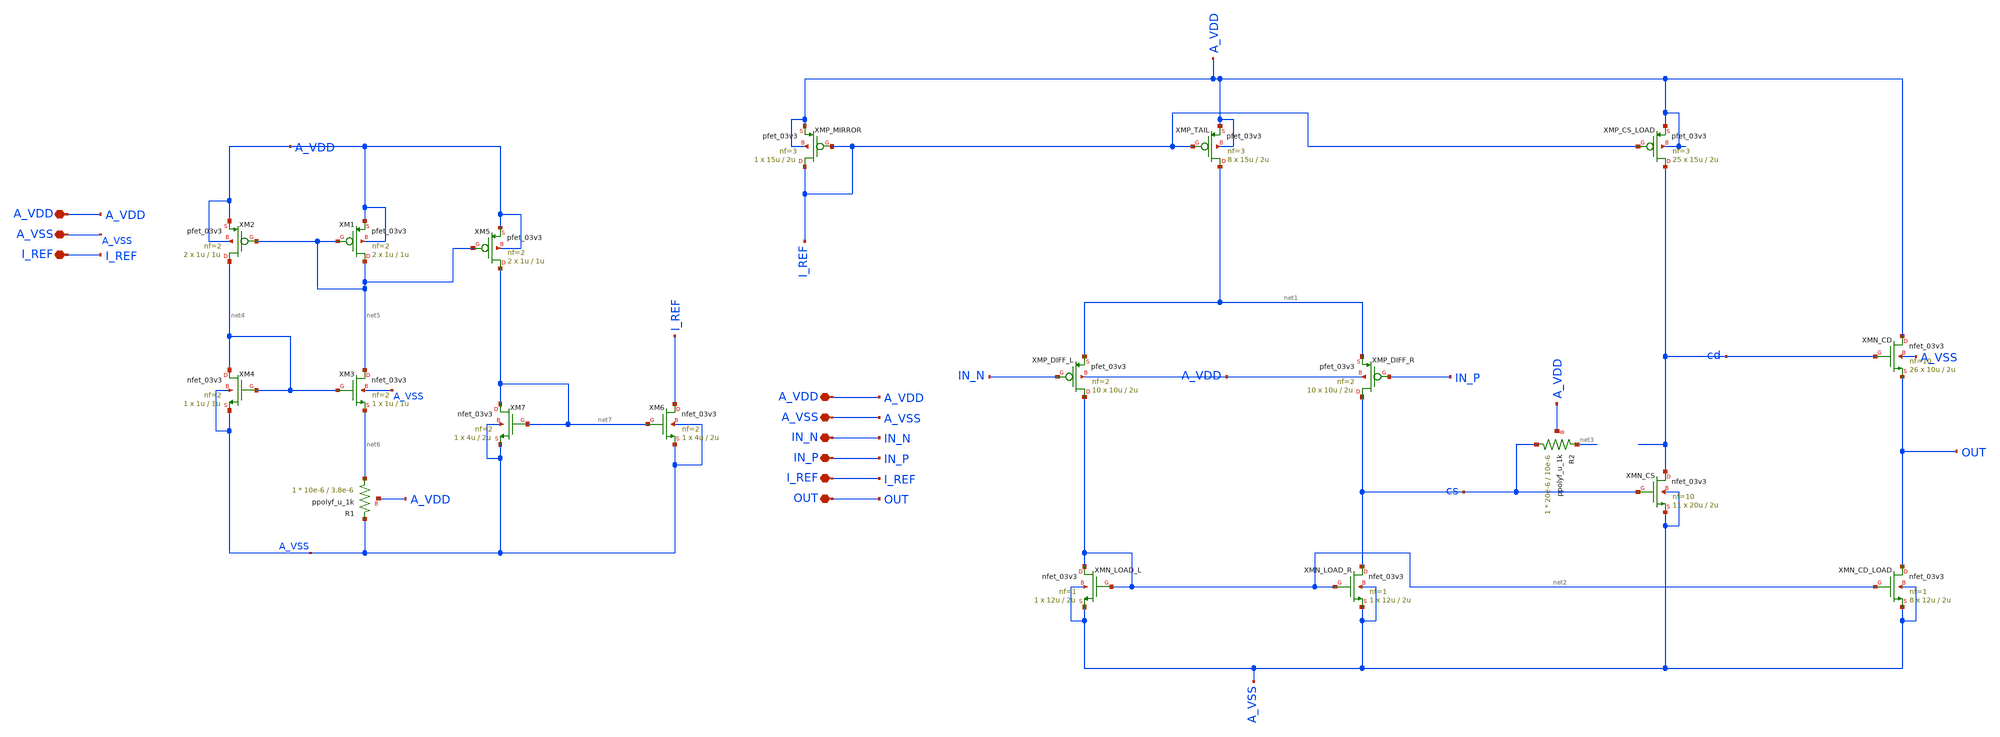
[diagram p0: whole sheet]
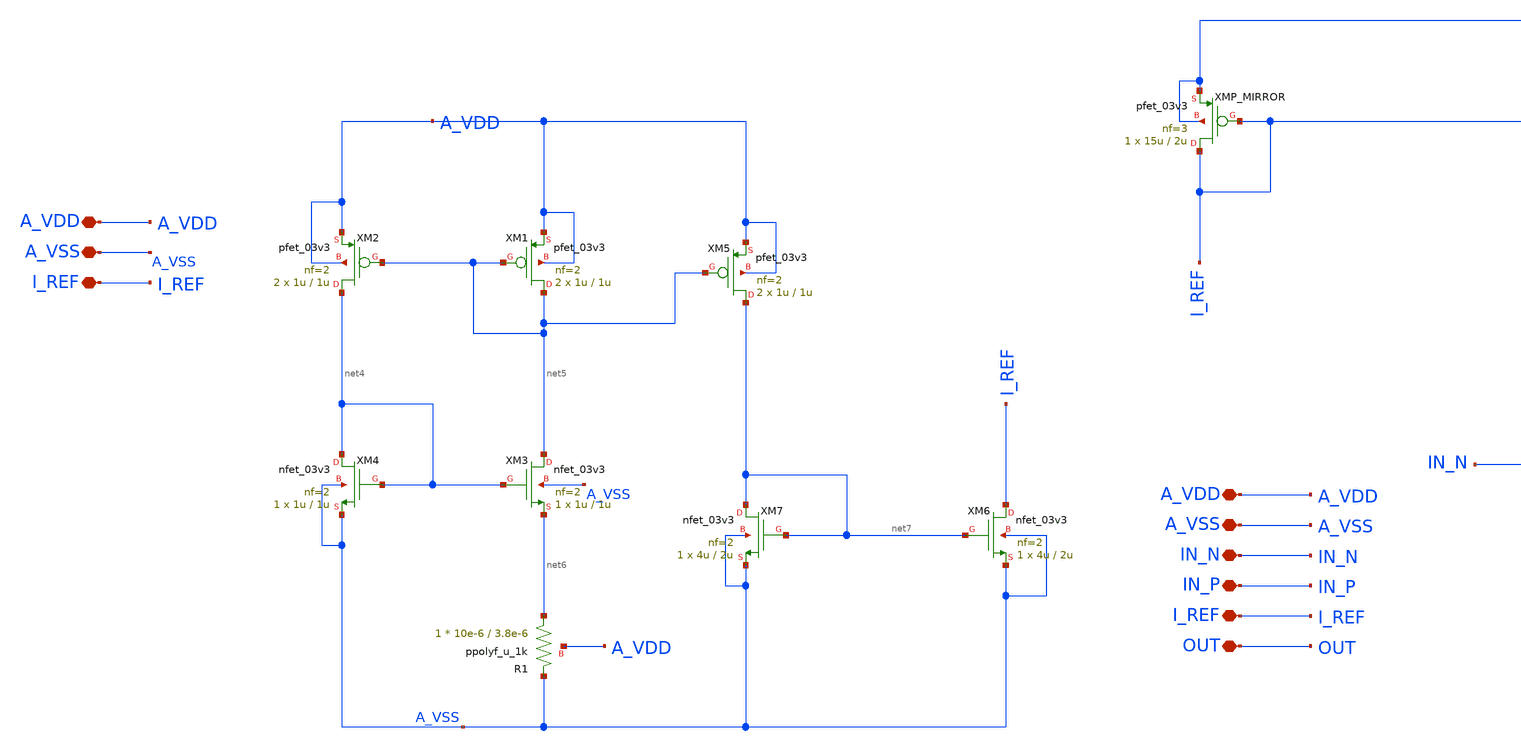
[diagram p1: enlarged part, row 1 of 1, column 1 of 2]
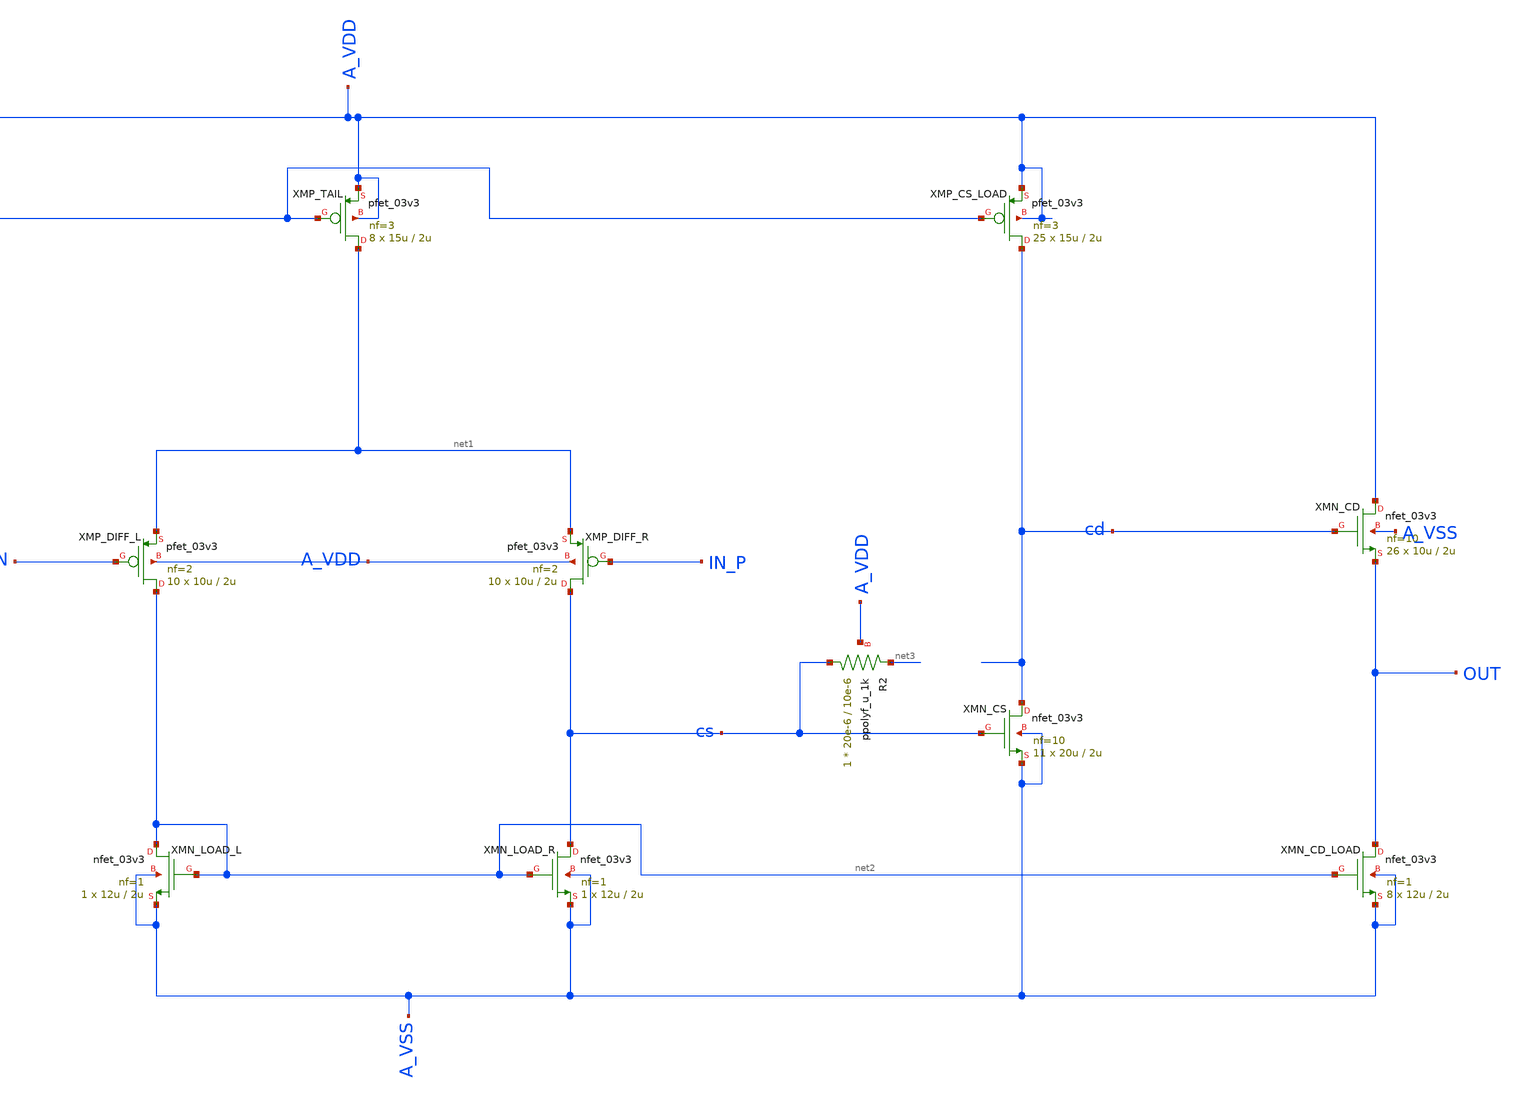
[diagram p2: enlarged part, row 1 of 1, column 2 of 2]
** sch_path: designs/libs/TIA/TIA_and_IREF.sch
**.subckt TIA_and_IREF A_VDD IN_N IN_P A_VSS I_REF OUT I_REF A_VSS A_VDD
*.iopin A_VDD
*.iopin IN_N
*.iopin IN_P
*.iopin A_VSS
*.iopin I_REF
*.iopin OUT
*.iopin I_REF
*.iopin A_VSS
*.iopin A_VDD
XMP_TAIL net1 I_REF A_VDD A_VDD pfet_03v3 L=2u W=15u nf=3 ad='int((nf+1)/2) * W/nf * 0.18u' as='int((nf+2)/2) * W/nf * 0.18u'
+ pd='2*int((nf+1)/2) * (W/nf + 0.18u)' ps='2*int((nf+2)/2) * (W/nf + 0.18u)' nrd='0.18u / W' nrs='0.18u / W'
+ sa=0 sb=0 sd=0 m=8
XMP_DIFF_L net2 IN_N net1 A_VDD pfet_03v3 L=2u W=10u nf=2 ad='int((nf+1)/2) * W/nf * 0.18u' as='int((nf+2)/2) * W/nf * 0.18u'
+ pd='2*int((nf+1)/2) * (W/nf + 0.18u)' ps='2*int((nf+2)/2) * (W/nf + 0.18u)' nrd='0.18u / W' nrs='0.18u / W'
+ sa=0 sb=0 sd=0 m=10
XMP_DIFF_R cs IN_P net1 A_VDD pfet_03v3 L=2u W=10u nf=2 ad='int((nf+1)/2) * W/nf * 0.18u' as='int((nf+2)/2) * W/nf * 0.18u'
+ pd='2*int((nf+1)/2) * (W/nf + 0.18u)' ps='2*int((nf+2)/2) * (W/nf + 0.18u)' nrd='0.18u / W' nrs='0.18u / W'
+ sa=0 sb=0 sd=0 m=10
XMP_CS_LOAD cd I_REF A_VDD A_VDD pfet_03v3 L=2u W=15u nf=3 ad='int((nf+1)/2) * W/nf * 0.18u' as='int((nf+2)/2) * W/nf * 0.18u'
+ pd='2*int((nf+1)/2) * (W/nf + 0.18u)' ps='2*int((nf+2)/2) * (W/nf + 0.18u)' nrd='0.18u / W' nrs='0.18u / W'
+ sa=0 sb=0 sd=0 m=25
XMP_MIRROR I_REF I_REF A_VDD A_VDD pfet_03v3 L=2u W=15u nf=3 ad='int((nf+1)/2) * W/nf * 0.18u' as='int((nf+2)/2) * W/nf * 0.18u'
+ pd='2*int((nf+1)/2) * (W/nf + 0.18u)' ps='2*int((nf+2)/2) * (W/nf + 0.18u)' nrd='0.18u / W' nrs='0.18u / W'
+ sa=0 sb=0 sd=0 m=1
XMN_LOAD_R cs net2 A_VSS A_VSS nfet_03v3 L=2u W=12u nf=1 ad='int((nf+1)/2) * W/nf * 0.18u' as='int((nf+2)/2) * W/nf * 0.18u'
+ pd='2*int((nf+1)/2) * (W/nf + 0.18u)' ps='2*int((nf+2)/2) * (W/nf + 0.18u)' nrd='0.18u / W' nrs='0.18u / W'
+ sa=0 sb=0 sd=0 m=1
XMN_LOAD_L net2 net2 A_VSS A_VSS nfet_03v3 L=2u W=12u nf=1 ad='int((nf+1)/2) * W/nf * 0.18u' as='int((nf+2)/2) * W/nf * 0.18u'
+ pd='2*int((nf+1)/2) * (W/nf + 0.18u)' ps='2*int((nf+2)/2) * (W/nf + 0.18u)' nrd='0.18u / W' nrs='0.18u / W'
+ sa=0 sb=0 sd=0 m=1
XMN_CS cd cs A_VSS A_VSS nfet_03v3 L=2u W=20u nf=10 ad='int((nf+1)/2) * W/nf * 0.18u' as='int((nf+2)/2) * W/nf * 0.18u'
+ pd='2*int((nf+1)/2) * (W/nf + 0.18u)' ps='2*int((nf+2)/2) * (W/nf + 0.18u)' nrd='0.18u / W' nrs='0.18u / W'
+ sa=0 sb=0 sd=0 m=11
XMN_CD A_VDD cd OUT A_VSS nfet_03v3 L=2u W=10u nf=10 ad='int((nf+1)/2) * W/nf * 0.18u' as='int((nf+2)/2) * W/nf * 0.18u'
+ pd='2*int((nf+1)/2) * (W/nf + 0.18u)' ps='2*int((nf+2)/2) * (W/nf + 0.18u)' nrd='0.18u / W' nrs='0.18u / W'
+ sa=0 sb=0 sd=0 m=26
XMN_CD_LOAD OUT net2 A_VSS A_VSS nfet_03v3 L=2u W=12u nf=1 ad='int((nf+1)/2) * W/nf * 0.18u' as='int((nf+2)/2) * W/nf * 0.18u'
+ pd='2*int((nf+1)/2) * (W/nf + 0.18u)' ps='2*int((nf+2)/2) * (W/nf + 0.18u)' nrd='0.18u / W' nrs='0.18u / W'
+ sa=0 sb=0 sd=0 m=8
XR2 cs net3 A_VDD ppolyf_u_1k r_width=20e-6 r_length=10e-6 m=1
XM1 net5 net5 A_VDD A_VDD pfet_03v3 L=1u W=1u nf=2 ad='int((nf+1)/2) * W/nf * 0.18u' as='int((nf+2)/2) * W/nf * 0.18u'
+ pd='2*int((nf+1)/2) * (W/nf + 0.18u)' ps='2*int((nf+2)/2) * (W/nf + 0.18u)' nrd='0.18u / W' nrs='0.18u / W'
+ sa=0 sb=0 sd=0 m=2
XM2 net4 net5 A_VDD A_VDD pfet_03v3 L=1u W=1u nf=2 ad='int((nf+1)/2) * W/nf * 0.18u' as='int((nf+2)/2) * W/nf * 0.18u'
+ pd='2*int((nf+1)/2) * (W/nf + 0.18u)' ps='2*int((nf+2)/2) * (W/nf + 0.18u)' nrd='0.18u / W' nrs='0.18u / W'
+ sa=0 sb=0 sd=0 m=2
XM3 net5 net4 net6 A_VSS nfet_03v3 L=1u W=1u nf=2 ad='int((nf+1)/2) * W/nf * 0.18u' as='int((nf+2)/2) * W/nf * 0.18u'
+ pd='2*int((nf+1)/2) * (W/nf + 0.18u)' ps='2*int((nf+2)/2) * (W/nf + 0.18u)' nrd='0.18u / W' nrs='0.18u / W'
+ sa=0 sb=0 sd=0 m=1
XM4 net4 net4 A_VSS A_VSS nfet_03v3 L=1u W=1u nf=2 ad='int((nf+1)/2) * W/nf * 0.18u' as='int((nf+2)/2) * W/nf * 0.18u'
+ pd='2*int((nf+1)/2) * (W/nf + 0.18u)' ps='2*int((nf+2)/2) * (W/nf + 0.18u)' nrd='0.18u / W' nrs='0.18u / W'
+ sa=0 sb=0 sd=0 m=1
XR1 net6 A_VSS A_VDD ppolyf_u_1k r_width=10e-6 r_length=3.8e-6 m=1
XM6 I_REF net7 A_VSS A_VSS nfet_03v3 L=2u W=4u nf=2 ad='int((nf+1)/2) * W/nf * 0.18u' as='int((nf+2)/2) * W/nf * 0.18u'
+ pd='2*int((nf+1)/2) * (W/nf + 0.18u)' ps='2*int((nf+2)/2) * (W/nf + 0.18u)' nrd='0.18u / W' nrs='0.18u / W'
+ sa=0 sb=0 sd=0 m=1
XM7 net7 net7 A_VSS A_VSS nfet_03v3 L=2u W=4u nf=2 ad='int((nf+1)/2) * W/nf * 0.18u' as='int((nf+2)/2) * W/nf * 0.18u'
+ pd='2*int((nf+1)/2) * (W/nf + 0.18u)' ps='2*int((nf+2)/2) * (W/nf + 0.18u)' nrd='0.18u / W' nrs='0.18u / W'
+ sa=0 sb=0 sd=0 m=1
XM5 net7 net5 A_VDD A_VDD pfet_03v3 L=1u W=1u nf=2 ad='int((nf+1)/2) * W/nf * 0.18u' as='int((nf+2)/2) * W/nf * 0.18u'
+ pd='2*int((nf+1)/2) * (W/nf + 0.18u)' ps='2*int((nf+2)/2) * (W/nf + 0.18u)' nrd='0.18u / W' nrs='0.18u / W'
+ sa=0 sb=0 sd=0 m=2
**.ends
.end
